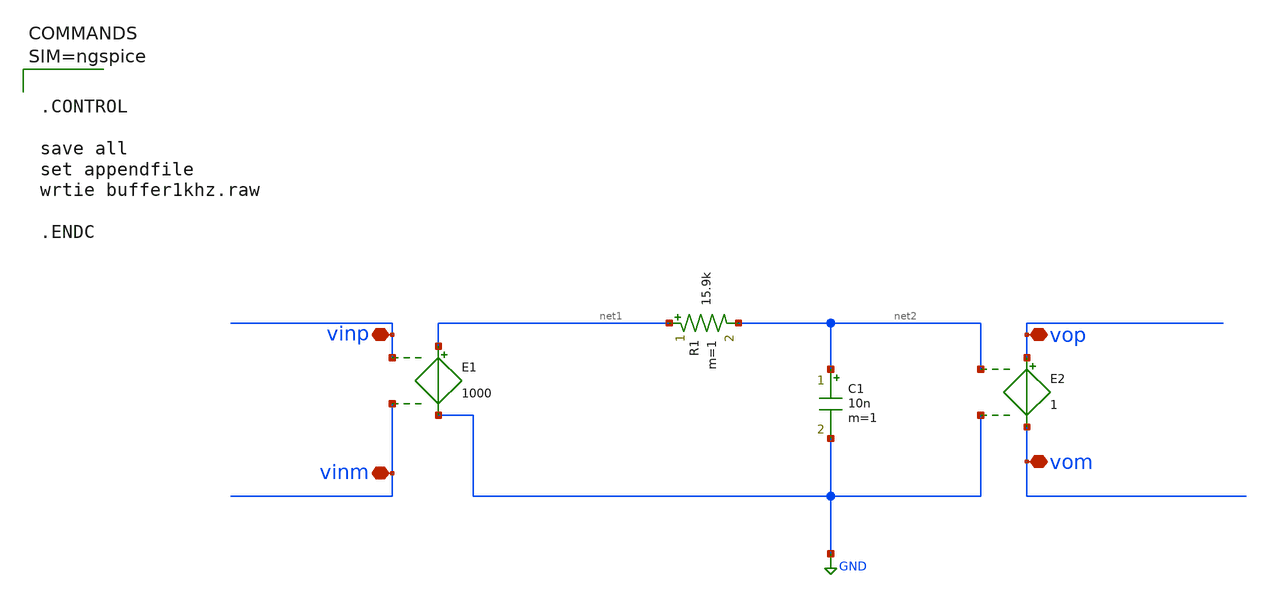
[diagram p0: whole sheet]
** sch_path: work/xschem/buffer1khz.sch
**.subckt buffer1khz vop vom vinp vinm
*.iopin vop
*.iopin vom
*.iopin vinp
*.iopin vinm
R1 net1 net2 15.9k m=1
C1 net2 GND 10n m=1
E1 net1 GND vinp vinm 1000
E2 vop vom net2 GND 1
**** begin user architecture code



.CONTROL

save all
set appendfile
wrtie buffer1khz.raw

.ENDC



**** end user architecture code
**.ends
.GLOBAL GND
.end
